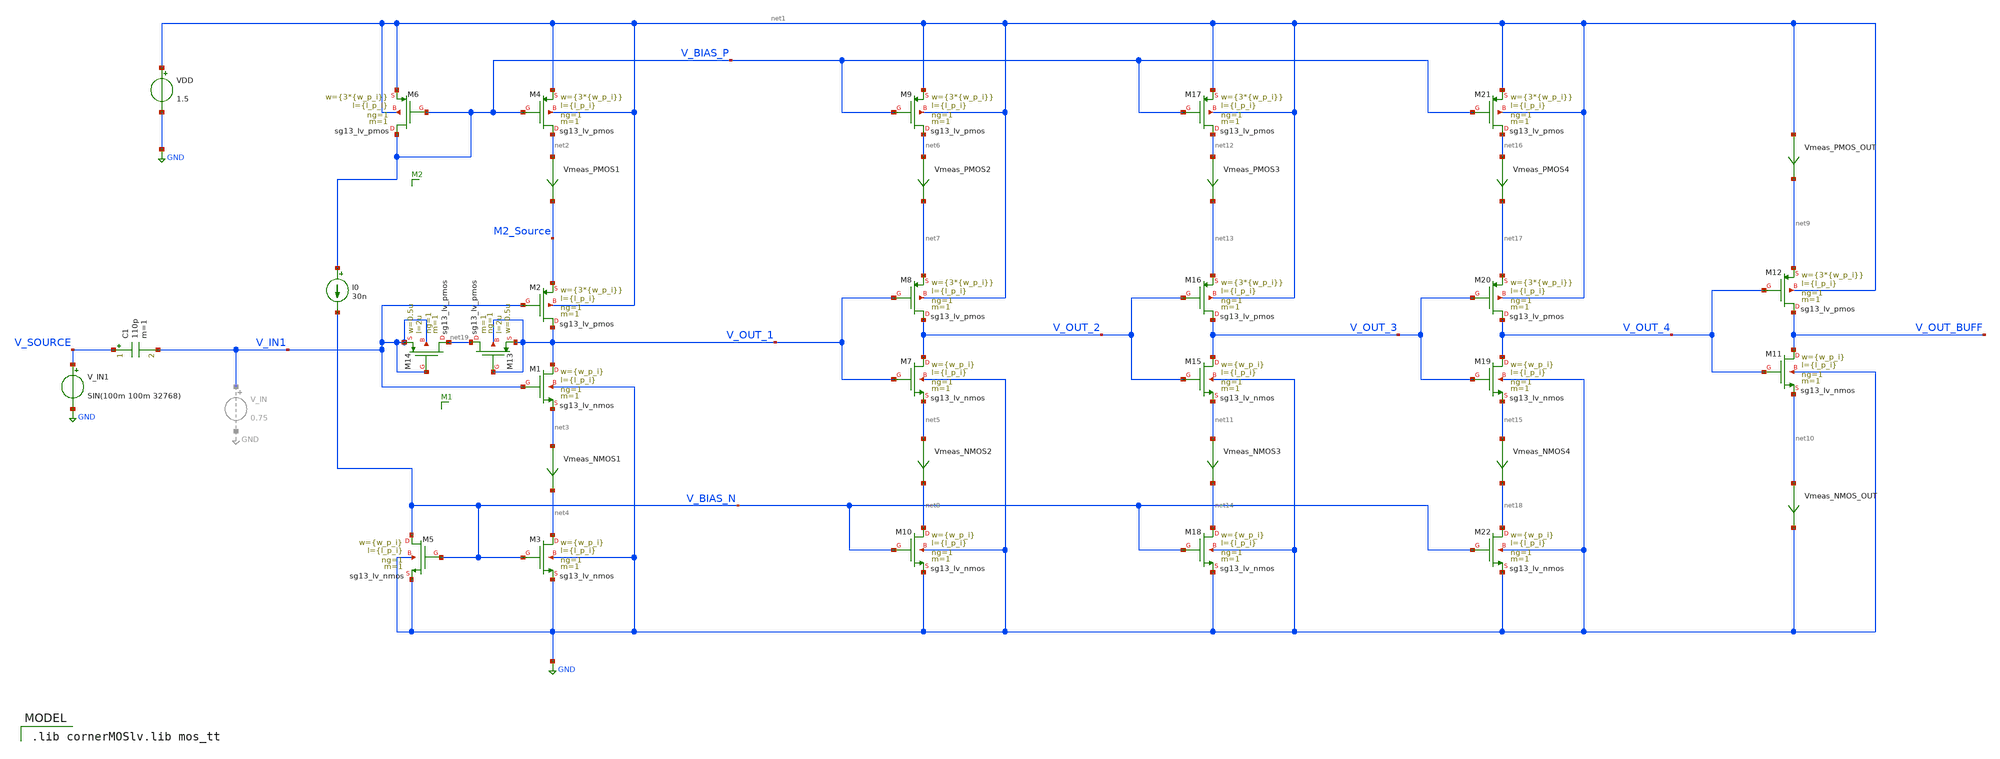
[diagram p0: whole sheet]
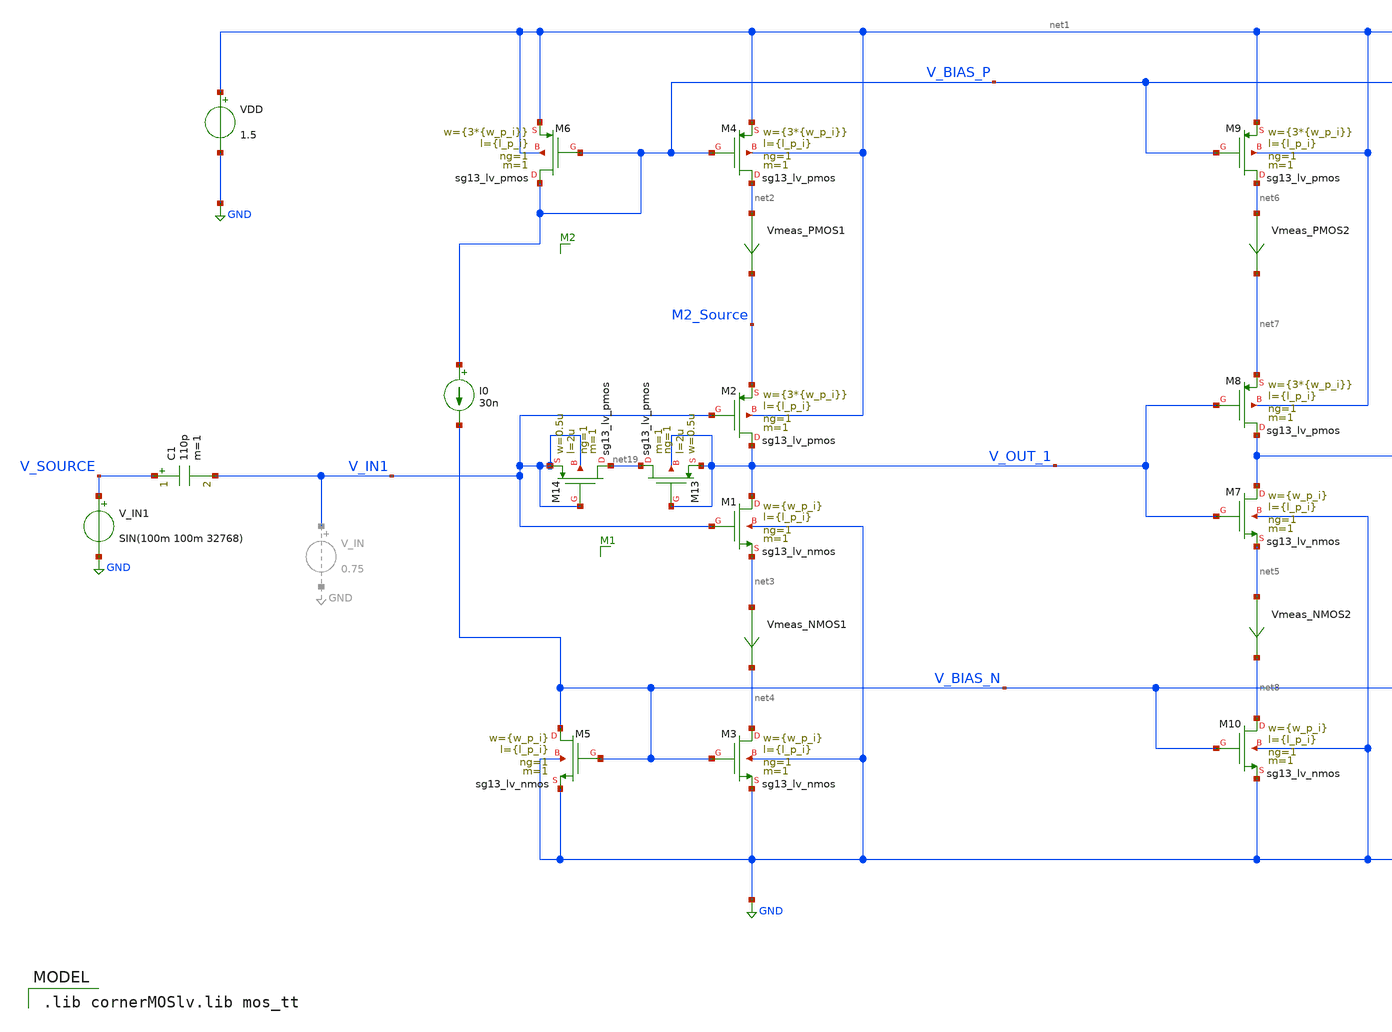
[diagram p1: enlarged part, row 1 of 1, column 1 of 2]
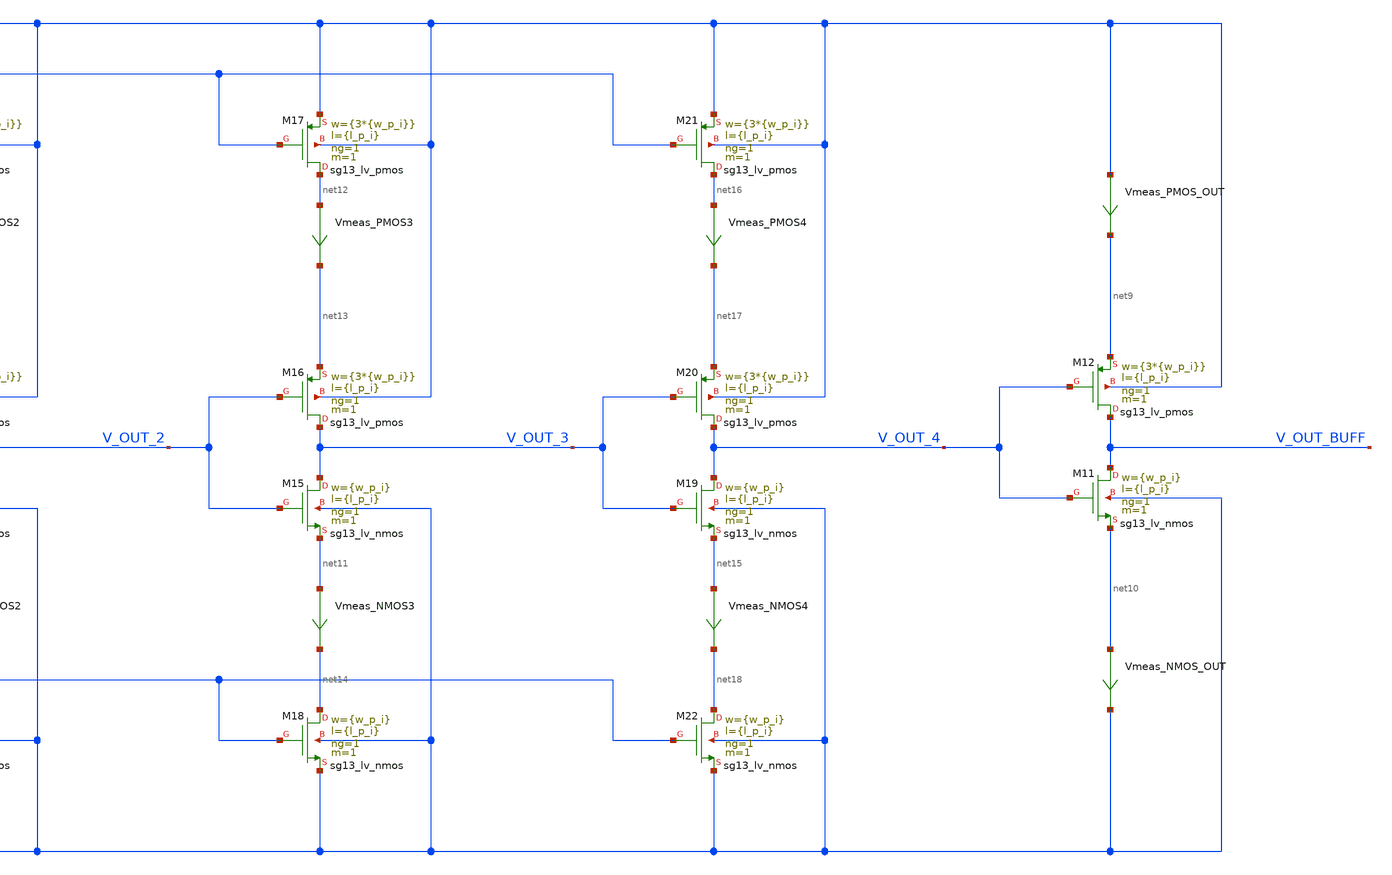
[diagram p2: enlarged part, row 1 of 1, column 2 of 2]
** sch_path: inverter_starved_v1_playground.sch
**.subckt inverter_starved_v1_playground
XM1 V_OUT_1 V_IN1 net3 GND sg13_lv_nmos w={w_p_i} l={l_p_i} ng=1 m=1 mm_ok=1
XM2 V_OUT_1 V_IN1 M2_Source net1 sg13_lv_pmos w={3*{w_p_i}} l={l_p_i} ng=1 m=1 mm_ok=1
VDD net1 GND 1.5
XM3 net4 V_BIAS_N GND GND sg13_lv_nmos w={w_p_i} l={l_p_i} ng=1 m=1 mm_ok=1
XM4 net2 V_BIAS_P net1 net1 sg13_lv_pmos w={3*{w_p_i}} l={l_p_i} ng=1 m=1 mm_ok=1
XM5 V_BIAS_N V_BIAS_N GND GND sg13_lv_nmos w={w_p_i} l={l_p_i} ng=1 m=1 mm_ok=1
XM6 V_BIAS_P V_BIAS_P net1 net1 sg13_lv_pmos w={3*{w_p_i}} l={l_p_i} ng=1 m=1 mm_ok=1
I0 V_BIAS_P V_BIAS_N 30n
Vmeas_PMOS1 net2 M2_Source 0
.save i(vmeas_pmos1)
Vmeas_NMOS1 net3 net4 0
.save i(vmeas_nmos1)
V_IN1 V_SOURCE GND SIN(100m 100m 32768)
C1 V_SOURCE V_IN1 110p m=1
XM7 V_OUT_2 V_OUT_1 net5 GND sg13_lv_nmos w={w_p_i} l={l_p_i} ng=1 m=1 mm_ok=1
XM8 V_OUT_2 V_OUT_1 net7 net1 sg13_lv_pmos w={3*{w_p_i}} l={l_p_i} ng=1 m=1 mm_ok=1
Vmeas_NMOS2 net5 net8 0
.save i(vmeas_nmos2)
XM9 net6 V_BIAS_P net1 net1 sg13_lv_pmos w={3*{w_p_i}} l={l_p_i} ng=1 m=1 mm_ok=1
Vmeas_PMOS2 net6 net7 0
.save i(vmeas_pmos2)
XM10 net8 V_BIAS_N GND GND sg13_lv_nmos w={w_p_i} l={l_p_i} ng=1 m=1 mm_ok=1
XM11 V_OUT_BUFF V_OUT_4 net10 GND sg13_lv_nmos w={w_p_i} l={l_p_i} ng=1 m=1 mm_ok=1
XM12 V_OUT_BUFF V_OUT_4 net9 net1 sg13_lv_pmos w={3*{w_p_i}} l={l_p_i} ng=1 m=1 mm_ok=1
XM13 net19 V_OUT_1 V_OUT_1 V_OUT_1 sg13_lv_pmos w=0.5u l=2u ng=1 m=1 mm_ok=1
XM14 net19 V_IN1 V_IN1 V_IN1 sg13_lv_pmos w=0.5u l=2u ng=1 m=1 mm_ok=1
Vmeas_PMOS_OUT net1 net9 0
.save i(vmeas_pmos_out)
Vmeas_NMOS_OUT net10 GND 0
.save i(vmeas_nmos_out)
XM15 V_OUT_3 V_OUT_2 net11 GND sg13_lv_nmos w={w_p_i} l={l_p_i} ng=1 m=1 mm_ok=1
XM16 V_OUT_3 V_OUT_2 net13 net1 sg13_lv_pmos w={3*{w_p_i}} l={l_p_i} ng=1 m=1 mm_ok=1
Vmeas_NMOS3 net11 net14 0
.save i(vmeas_nmos3)
XM17 net12 V_BIAS_P net1 net1 sg13_lv_pmos w={3*{w_p_i}} l={l_p_i} ng=1 m=1 mm_ok=1
Vmeas_PMOS3 net12 net13 0
.save i(vmeas_pmos3)
XM18 net14 V_BIAS_N GND GND sg13_lv_nmos w={w_p_i} l={l_p_i} ng=1 m=1 mm_ok=1
XM19 V_OUT_4 V_OUT_3 net15 GND sg13_lv_nmos w={w_p_i} l={l_p_i} ng=1 m=1 mm_ok=1
XM20 V_OUT_4 V_OUT_3 net17 net1 sg13_lv_pmos w={3*{w_p_i}} l={l_p_i} ng=1 m=1 mm_ok=1
Vmeas_NMOS4 net15 net18 0
.save i(vmeas_nmos4)
XM21 net16 V_BIAS_P net1 net1 sg13_lv_pmos w={3*{w_p_i}} l={l_p_i} ng=1 m=1 mm_ok=1
Vmeas_PMOS4 net16 net17 0
.save i(vmeas_pmos4)
XM22 net18 V_BIAS_N GND GND sg13_lv_nmos w={w_p_i} l={l_p_i} ng=1 m=1 mm_ok=1
**** begin user architecture code
 .lib cornerMOSlv.lib mos_tt



.include inverter_starved_playground.save
*.param w_p_i=0.4u l_p_i=0.13u
*.param w_p_i=0.65u l_p_i=0.145u
.param w_p_i=0.35u l_p_i=0.14u
.param w_p=0.4u l_p=0.13u
.meas tran iavg_stage_1_pmos AVG i(Vmeas_PMOS1)
.meas tran iavg_stage_1_nmos AVG i(Vmeas_NMOS1)
.meas tran iavg_stage_2_pmos AVG i(Vmeas_PMOS2)
.meas tran iavg_stage_2_nmos AVG i(Vmeas_NMOS2)
.meas tran iavg_stage_3_pmos AVG i(Vmeas_PMOS3)
.meas tran iavg_stage_3_nmos AVG i(Vmeas_NMOS3)
.meas tran iavg_stage_4_pmos AVG i(Vmeas_PMOS4)
.meas tran iavg_stage_4_nmos AVG i(Vmeas_NMOS4)
.meas tran iavg_stage_5_pmos AVG i(Vmeas_PMOS_OUT)
.meas tran iavg_stage_5_nmos AVG i(Vmeas_NMOS_OUT)
.meas tran iavg_VDD AVG i(VDD)

.control
save all
*save V_SOURCE V_OUT_BUFF

op
write inverter_starved_v1_playground.raw
set appendwrite

tran 0.01u 0.5m

plot V_SOURCE V_IN1 V_OUT_1 V_OUT_2 V_OUT_3 V_OUT_4 V_OUT_BUFF
*plot V_IN1 V_OUT_1 V_OUT_BUFF


*linearize V_OUT_BUFF
*fft V_OUT_BUFF
*plot mag(V_OUT_BUFF)

*.measure tran yrms RMS i(VDD) from=0.1m to=0.2m

.endc


**** end user architecture code
**.ends
.GLOBAL GND
.end
